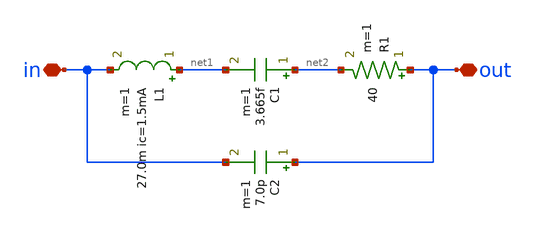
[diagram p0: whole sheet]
** sch_path: xschem/resonator_32k.sch
**.subckt resonator_32k out in
*.iopin out
*.iopin in
L1 net1 in 27.0m ic=1.5mA m=1
C1 net2 net1 3.665f m=1
C2 out in 7.0p m=1
R1 out net2 40 m=1
**.ends
.end
